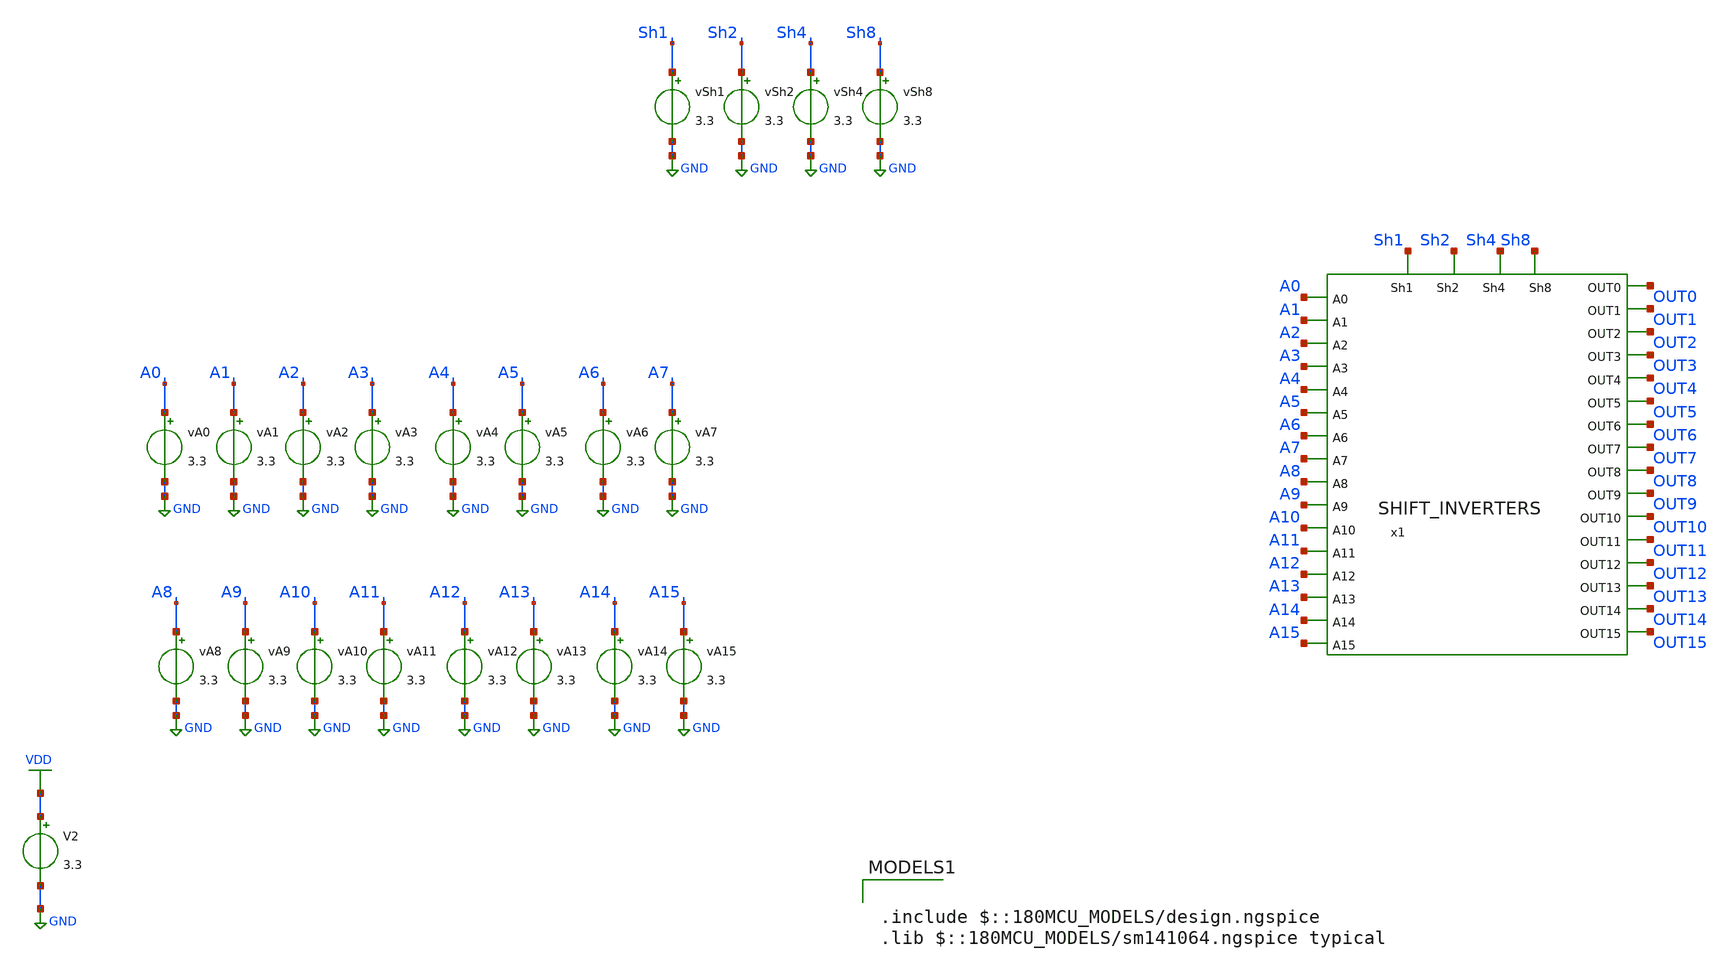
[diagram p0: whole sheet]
** sch_path: tbs/shift_tb.sch
**.subckt shift_tb
x1 OUT0 Sh1 OUT1 OUT2 Sh2 OUT3 OUT4 A0 OUT5 A1 OUT6 Sh4 OUT7 OUT8 A2 A3 OUT9 OUT10 OUT11 Sh8 OUT12
+ A4 OUT13 A5 A6 OUT14 A7 OUT15 A8 A9 A10 A11 A12 A13 A14 A15 SHIFT_INVERTERS
vA0 A0 GND 3.3
vA1 A1 GND 3.3
vA2 A2 GND 3.3
vA3 A3 GND 3.3
vA4 A4 GND 3.3
vA5 A5 GND 3.3
vA6 A6 GND 3.3
vA7 A7 GND 3.3
vA8 A8 GND 3.3
vA9 A9 GND 3.3
vA10 A10 GND 3.3
vA11 A11 GND 3.3
vA12 A12 GND 3.3
vA13 A13 GND 3.3
vA14 A14 GND 3.3
vA15 A15 GND 3.3
vSh1 Sh1 GND 3.3
vSh2 Sh2 GND 3.3
vSh4 Sh4 GND 3.3
vSh8 Sh8 GND 3.3
V2 VDD GND 3.3
**** begin user architecture code

.include $::180MCU_MODELS/design.ngspice
.lib $::180MCU_MODELS/sm141064.ngspice typical



.control
let vlow = 0
let vhigh = 3.3

* A = 1010101010101010 = 43690
alter VA15 = $&vhigh
alter VA14 = $&vlow
alter VA13 = $&vhigh
alter VA12 = $&vlow
alter VA11 = $&vhigh
alter VA10 = $&vlow
alter VA9  = $&vhigh
alter VA8  = $&vlow
alter VA7  = $&vhigh
alter VA6  = $&vlow
alter VA5  = $&vhigh
alter VA4  = $&vlow
alter VA3  = $&vhigh
alter VA2  = $&vlow
alter VA1  = $&vhigh
alter VA0  = $&vlow

* --- Define Shift Control Values ---
* Setting Sh1 high, others low (Shift 1)
alter vSh8 = $&vlow
alter vSh4 = $&vlow
alter vSh2 = $&vlow
alter vSh1 = $&vhigh

* Run transient
tran 1n 40n

* --- Digitizing each bit (Measurement at 30ns) ---
meas tran v0  find v(OUT0)  at=30n
meas tran v1  find v(OUT1)  at=30n
meas tran v2  find v(OUT2)  at=30n
meas tran v3  find v(OUT3)  at=30n
meas tran v4  find v(OUT4)  at=30n
meas tran v5  find v(OUT5)  at=30n
meas tran v6  find v(OUT6)  at=30n
meas tran v7  find v(OUT7)  at=30n
meas tran v8  find v(OUT8)  at=30n
meas tran v9  find v(OUT9)  at=30n
meas tran v10 find v(OUT10) at=30n
meas tran v11 find v(OUT11) at=30n
meas tran v12 find v(OUT12) at=30n
meas tran v13 find v(OUT13) at=30n
meas tran v14 find v(OUT14) at=30n
meas tran v15 find v(OUT15) at=30n

* Initialize tracking variables
let decimal_result = 0

* Logic checks (Standard threshold 1.6V)
if v0 > 1.6
  let decimal_result = decimal_result + 1
end
if v1 > 1.6
  let decimal_result = decimal_result + 2
end
if v2 > 1.6
  let decimal_result = decimal_result + 4
end
if v3 > 1.6
  let decimal_result = decimal_result + 8
end
if v4 > 1.6
  let decimal_result = decimal_result + 16
end
if v5 > 1.6
  let decimal_result = decimal_result + 32
end
if v6 > 1.6
  let decimal_result = decimal_result + 64
end
if v7 > 1.6
  let decimal_result = decimal_result + 128
end
if v8 > 1.6
  let decimal_result = decimal_result + 256
end
if v9 > 1.6
  let decimal_result = decimal_result + 512
end
if v10 > 1.6
  let decimal_result = decimal_result + 1024
end
if v11 > 1.6
  let decimal_result = decimal_result + 2048
end
if v12 > 1.6
  let decimal_result = decimal_result + 4096
end
if v13 > 1.6
  let decimal_result = decimal_result + 8192
end
if v14 > 1.6
  let decimal_result = decimal_result + 16384
end
if v15 > 1.6
  let decimal_result = decimal_result + 32768
end

* --- Output Results ---
echo hello?
print decimal_result
.endc


**** end user architecture code
**.ends
.GLOBAL GND
.GLOBAL VDD
.end
